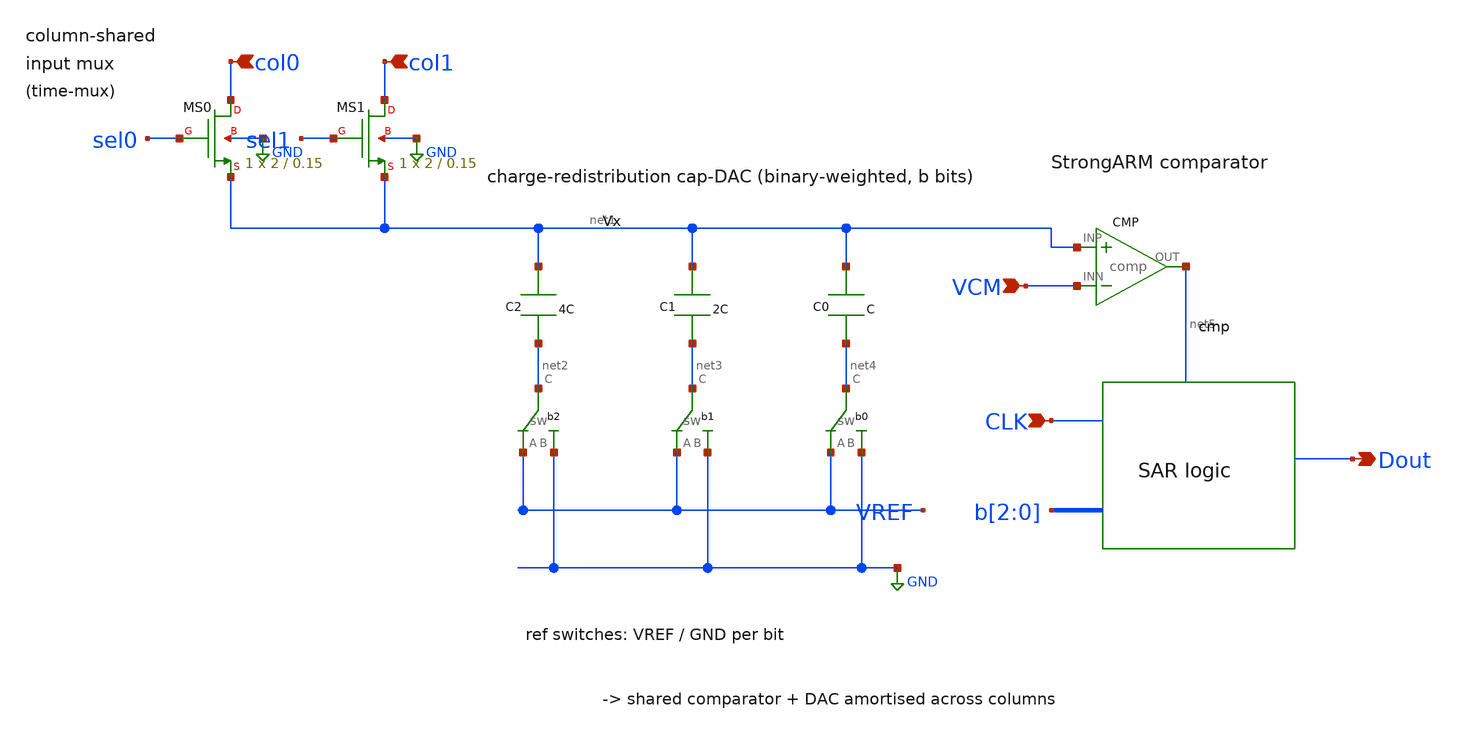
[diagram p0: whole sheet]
** sch_path: eda/hero/schematics/sar_readout.sch
**.subckt sar_readout col0 col1 VCM CLK Dout
*.ipin col0
*.ipin col1
*.ipin VCM
*.ipin CLK
*.opin Dout
XMS0 col0 sel0 net1 GND sky130_fd_pr__sky130_fd_pr__nfet_01v8 L=0.15 W=2 nrd='0.29 / W' nrs='0.29 / W'
+ sa=0 sb=0 sd=0 mult=1 m=1
XMS1 col1 sel1 net1 GND sky130_fd_pr__sky130_fd_pr__nfet_01v8 L=0.15 W=2 nrd='0.29 / W' nrs='0.29 / W'
+ sa=0 sb=0 sd=0 mult=1 m=1
C2 net1 net2 4C m=1
C1 net1 net3 2C m=1
C0 net1 net4 C m=1
**.ends
.GLOBAL GND
.end
